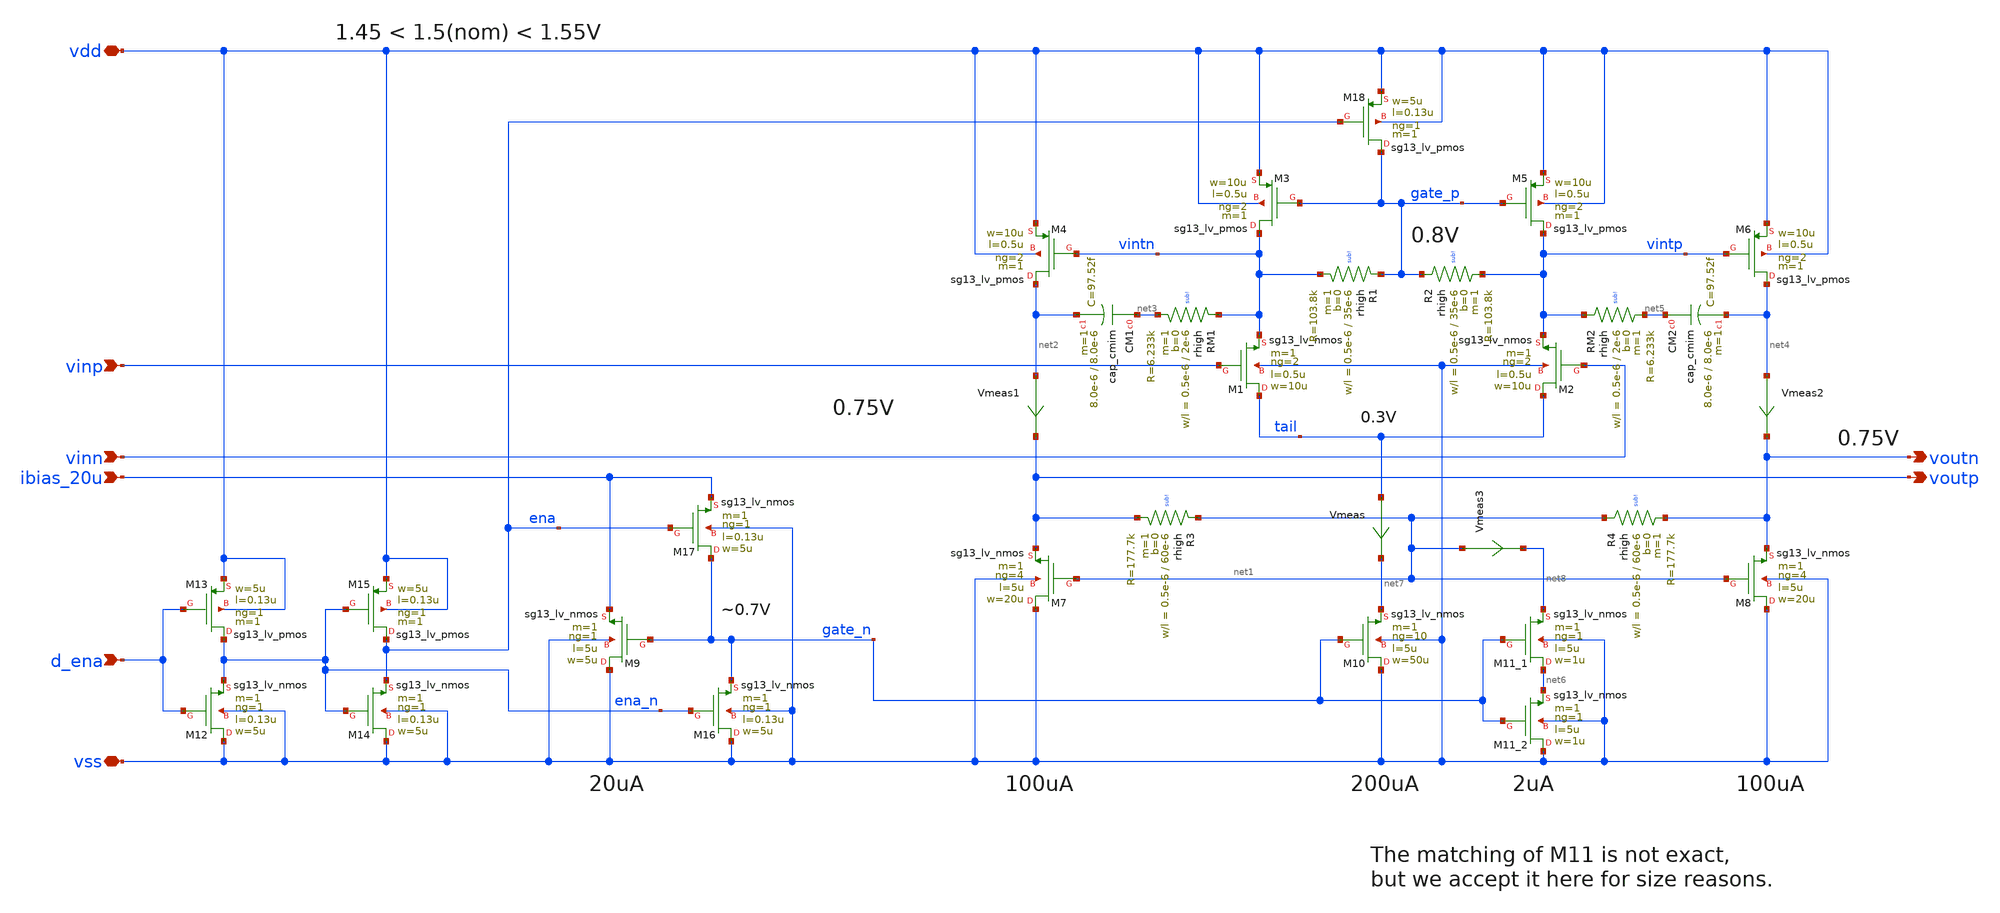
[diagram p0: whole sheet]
** sch_path: xschem/ota-diff.sch
* (c) 2025 H. Pretl, Apache-2.0 license
**.subckt ota-diff ibias_20u vdd vss vinp vinn voutp d_ena voutn
*.ipin ibias_20u
*.iopin vdd
*.iopin vss
*.ipin vinp
*.ipin vinn
*.opin voutp
*.ipin d_ena
*.opin voutn
XM10 vss gate_n net7 vss sg13_lv_nmos w=50u l=5u ng=10 m=1 mm_ok=1
XM1 tail vinp vintn vss sg13_lv_nmos w=10u l=0.5u ng=2 m=1 mm_ok=1
XM2 tail vinn vintp vss sg13_lv_nmos w=10u l=0.5u ng=2 m=1 mm_ok=1
XM3 vintn gate_p vdd vdd sg13_lv_pmos w=10u l=0.5u ng=2 m=1 mm_ok=1
XM9 vss gate_n ibias_20u vss sg13_lv_nmos w=5u l=5u ng=1 m=1 mm_ok=1
XM16 vss ena_n gate_n vss sg13_lv_nmos w=5u l=0.13u ng=1 m=1 mm_ok=1
XM18 gate_p ena vdd vdd sg13_lv_pmos w=5u l=0.13u ng=1 m=1 mm_ok=1
XM14 vss ena_n ena vss sg13_lv_nmos w=5u l=0.13u ng=1 m=1 mm_ok=1
XM15 ena ena_n vdd vdd sg13_lv_pmos w=5u l=0.13u ng=1 m=1 mm_ok=1
XM17 gate_n ena ibias_20u vss sg13_lv_nmos w=5u l=0.13u ng=1 m=1 mm_ok=1
XM12 vss d_ena ena_n vss sg13_lv_nmos w=5u l=0.13u ng=1 m=1 mm_ok=1
XM13 ena_n d_ena vdd vdd sg13_lv_pmos w=5u l=0.13u ng=1 m=1 mm_ok=1
XM7 vss net1 voutp vss sg13_lv_nmos w=20u l=5u ng=4 m=1 mm_ok=1
XR1 gate_p vintn sub! rhigh w=0.5e-6 l=35e-6 m=1 b=0 mm_ok=1
XR3 net1 voutp sub! rhigh w=0.5e-6 l=60e-6 m=1 b=0 mm_ok=1
XM11_1 net6 gate_n net8 vss sg13_lv_nmos w=1u l=5u ng=1 m=1 mm_ok=1
XRM1 vintn net3 sub! rhigh w=0.5e-6 l=2e-6 m=1 b=0 mm_ok=1
XCM1 net3 net2 cap_cmim w=8.0e-6 l=8.0e-6 m=1 mm_ok=1
XM5 vintp gate_p vdd vdd sg13_lv_pmos w=10u l=0.5u ng=2 m=1 mm_ok=1
XM4 net2 vintn vdd vdd sg13_lv_pmos w=10u l=0.5u ng=2 m=1 mm_ok=1
XM6 net4 vintp vdd vdd sg13_lv_pmos w=10u l=0.5u ng=2 m=1 mm_ok=1
XR2 gate_p vintp sub! rhigh w=0.5e-6 l=35e-6 m=1 b=0 mm_ok=1
XRM2 vintp net5 sub! rhigh w=0.5e-6 l=2e-6 m=1 b=0 mm_ok=1
XCM2 net5 net4 cap_cmim w=8.0e-6 l=8.0e-6 m=1 mm_ok=1
XM8 vss net1 voutn vss sg13_lv_nmos w=20u l=5u ng=4 m=1 mm_ok=1
XM11_2 vss gate_n net6 vss sg13_lv_nmos w=1u l=5u ng=1 m=1 mm_ok=1
XR4 net1 voutn sub! rhigh w=0.5e-6 l=60e-6 m=1 b=0 mm_ok=1
Vmeas tail net7 0
.save i(vmeas)
Vmeas1 net2 voutp 0
.save i(vmeas1)
Vmeas2 net4 voutn 0
.save i(vmeas2)
Vmeas3 net1 net8 0
.save i(vmeas3)
**.ends
.end
